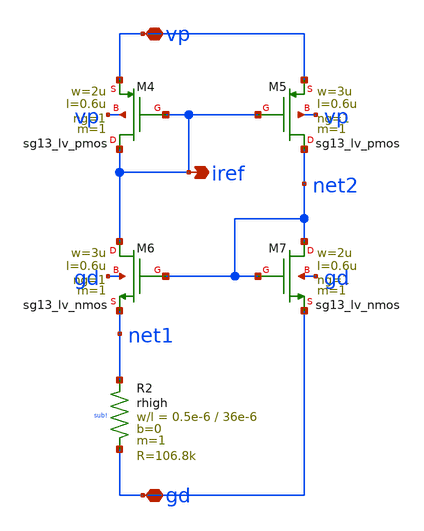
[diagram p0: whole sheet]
** sch_path: charge_pump/curr_source.sch
**.subckt curr_source vp gd iref
*.iopin vp
*.iopin gd
*.opin iref
XM4 iref iref vp vp sg13_lv_pmos w=2u l=0.6u ng=1 m=1 mm_ok=1
XM5 net2 iref vp vp sg13_lv_pmos w=3u l=0.6u ng=1 m=1 mm_ok=1
XM6 iref net2 net1 gd sg13_lv_nmos w=3u l=0.6u ng=1 m=1 mm_ok=1
XM7 net2 net2 gd gd sg13_lv_nmos w=2u l=0.6u ng=1 m=1 mm_ok=1
XR2 net1 gd sub! rhigh w=0.5e-6 l=36e-6 m=1 b=0 mm_ok=1
**.ends
.end
